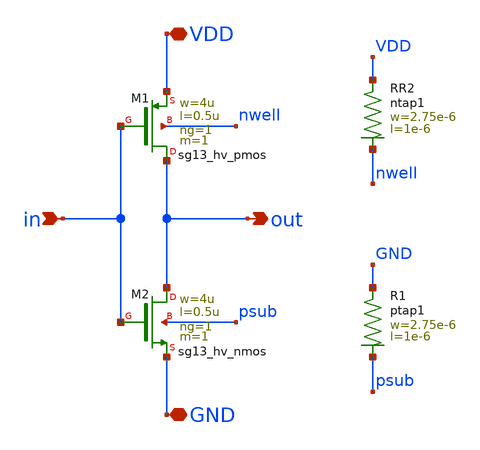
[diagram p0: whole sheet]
** sch_path: xschem/inv.sch
**.subckt inv in VDD GND out
*.ipin in
*.iopin VDD
*.iopin GND
*.opin out
XM1 out in VDD nwell sg13_hv_pmos w=4u l=0.5u ng=1 m=1 mm_ok=1
XM2 out in GND psub sg13_hv_nmos w=4u l=0.5u ng=1 m=1 mm_ok=1
XR1 GND psub ptap1 R=95.61 w=2.75e-6 l=1e-6
XR2 VDD nwell ntap1 R=95.61 w=2.75e-6 l=1e-6
**.ends
.end
